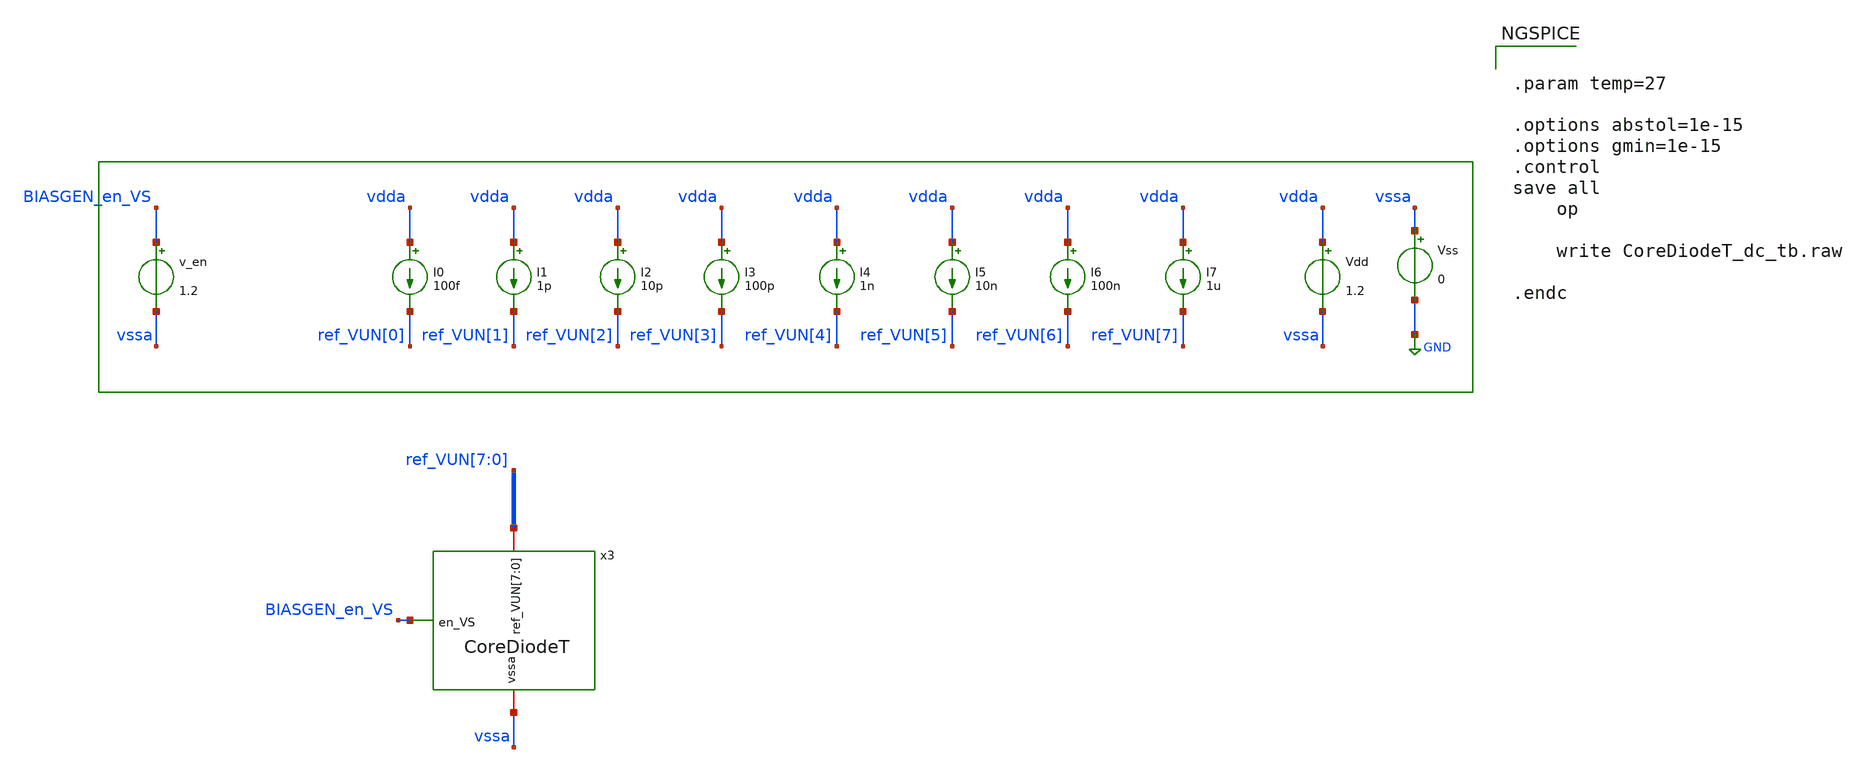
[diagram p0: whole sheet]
** sch_path: test_bench/CoreDiodeT_dc_tb.sch
**.subckt CoreDiodeT_dc_tb
v_en BIASGEN_en_VS vssa 1.2
Vdd vdda vssa 1.2
Vss vssa GND 0
I0 vdda ref_VUN[0] 100f
I1 vdda ref_VUN[1] 1p
I2 vdda ref_VUN[2] 10p
I3 vdda ref_VUN[3] 100p
I4 vdda ref_VUN[4] 1n
I6 vdda ref_VUN[6] 100n
I5 vdda ref_VUN[5] 10n
I7 vdda ref_VUN[7] 1u
x3 ref_VUN[7] ref_VUN[6] ref_VUN[5] ref_VUN[4] ref_VUN[3] ref_VUN[2] ref_VUN[1] ref_VUN[0] vssa
+ BIASGEN_en_VS CoreDiodeT
**** begin user architecture code

.lib cornerMOShv.lib mos_tt



.param temp=27

.options abstol=1e-15
.options gmin=1e-15
.control
save all
    op

    write CoreDiodeT_dc_tb.raw

.endc


**** end user architecture code
**.ends

* expanding   symbol:  CoreDiodeT.sym # of pins=3
** sym_path: test_bench/CoreDiodeT.sym
** sch_path: test_bench/CoreDiodeT.sch
.subckt CoreDiodeT ref_VUN[7] ref_VUN[6] ref_VUN[5] ref_VUN[4] ref_VUN[3] ref_VUN[2] ref_VUN[1]
+ ref_VUN[0] vssa en_VS
*.iopin ref_VUN[7],ref_VUN[6],ref_VUN[5],ref_VUN[4],ref_VUN[3],ref_VUN[2],ref_VUN[1],ref_VUN[0]
*.ipin en_VS
*.iopin vssa
x1 net8 vssa en_VS net8 ISINK
x2 net7 vssa en_VS net7 ISINK
x3 net1 vssa en_VS net1 ISINK
x4 net2 vssa en_VS net2 ISINK
x5 net3 vssa en_VS net3 ISINK
x6 net4 vssa en_VS net4 ISINK
x7 net5 vssa en_VS net5 ISINK
x8 net6 vssa en_VS net6 ISINK
C0 net6 vssa 2p m=1
C1 net5 vssa 2p m=1
C2 net4 vssa 2p m=1
C3 net3 vssa 2p m=1
C4 net2 vssa 2p m=1
C5 net1 vssa 2p m=1
C6 net7 vssa 2p m=1
C7 net8 vssa 2p m=1
V_ref_u_0 ref_VUN[0] net6 0
V_ref_u_1 ref_VUN[1] net5 0
V_ref_u_2 ref_VUN[2] net4 0
V_ref_u_3 ref_VUN[3] net3 0
V_ref_u_4 ref_VUN[4] net2 0
V_ref_u_5 ref_VUN[5] net1 0
V_ref_u_6 ref_VUN[6] net7 0
V_ref_u_7 ref_VUN[7] net8 0
.ends


* expanding   symbol:  ISINK.sym # of pins=4
** sym_path: test_bench/ISINK.sym
** sch_path: test_bench/ISINK.sch
.subckt ISINK bias_VN vssa en_VS io_UN
*.ipin en_VS
*.iopin vssa
*.ipin bias_VN
*.iopin io_UN
XM1 io_UN en_VS net2 vssa sg13_hv_nmos w=2.5u l=0.5u ng=1 m=1 mm_ok=1
XM2 net2 bias_VN net1 vssa sg13_hv_nmos w=1u l=2u ng=1 m=1 mm_ok=1
XM3 net1 bias_VN vssa vssa sg13_hv_nmos w=1u l=2u ng=1 m=1 mm_ok=1
.ends

.GLOBAL GND
.end
